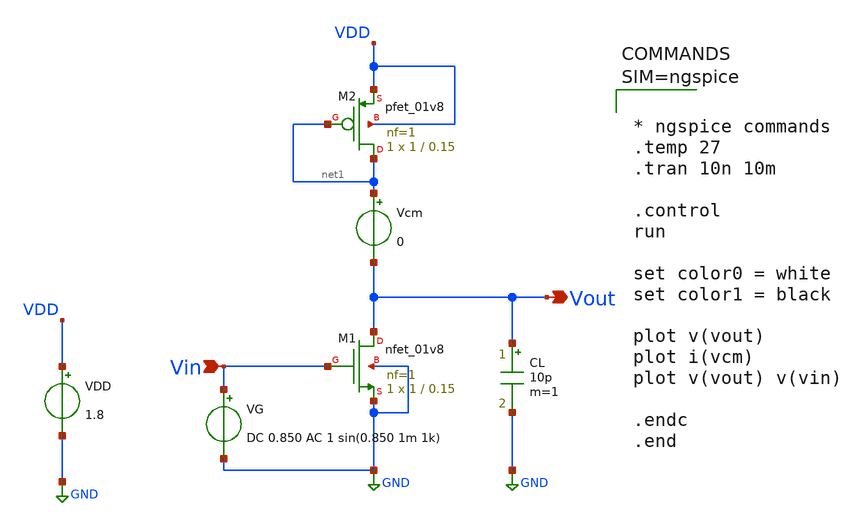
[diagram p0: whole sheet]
** sch_path: Common_Source_PMOS_Load_ckts/CS_Amp_PMOS_Diode_Load_Ckts/NMOS_PMOS_Diode_Load_AC_Transient_Analysis.sch
**.subckt NMOS_PMOS_Diode_Load_AC_Transient_Analysis Vout Vin
*.opin Vout
*.ipin Vin
XM1 Vout Vin GND GND sky130_fd_pr__nfet_01v8 L=0.15 W=1 nf=1 ad='int((1 + 1)/2) * 1 / 1 * 0.29' as='int((1 + 2)/2) * 1 / 1 * 0.29'
+ pd='2*int((1 + 1)/2) * (1 / 1 + 0.29)' ps='2*int((1 + 2)/2) * (1 / 1 + 0.29)' nrd='0.29 / 1 ' nrs='0.29 / 1 '
+ sa=0 sb=0 sd=0 mult=1 m=1
XM2 net1 net1 VDD VDD sky130_fd_pr__pfet_01v8 L=0.15 W=1 nf=1 ad='int((1 + 1)/2) * 1 / 1 * 0.29' as='int((1 + 2)/2) * 1 / 1 * 0.29'
+ pd='2*int((1 + 1)/2) * (1 / 1 + 0.29)' ps='2*int((1 + 2)/2) * (1 / 1 + 0.29)' nrd='0.29 / 1 ' nrs='0.29 / 1 '
+ sa=0 sb=0 sd=0 mult=1 m=1
Vcm net1 Vout 0
CL Vout GND 10p m=1
VG Vin GND DC 0.850 AC 1 sin(0.850 1m 1k)
VDD VDD GND 1.8
**** begin user architecture code

** opencircuitdesign pdks install
.lib $::SKYWATER_MODELS/sky130.lib.spice tt




* ngspice commands
.temp 27
.tran 10n 10m

.control
run

set color0 = white
set color1 = black

plot v(vout)
plot i(vcm)
plot v(vout) v(vin)

.endc
.end



**** end user architecture code
**.ends
.GLOBAL GND
.end
